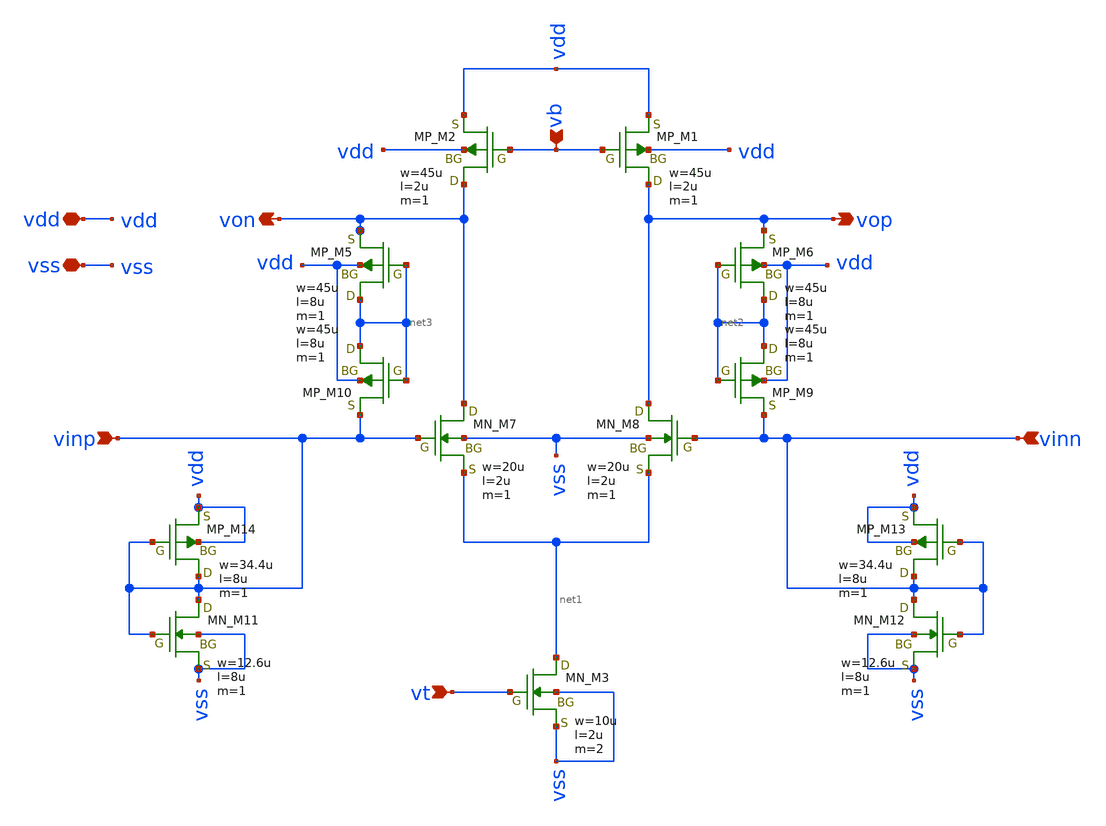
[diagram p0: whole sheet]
** sch_path: member_project/JJY_Receiver/Masahiro/jjy_recv/diff_amp/fully_diff_amp.sch
**.subckt fully_diff_amp vop von vinp vb vt vinn vdd vss
*.opin vop
*.opin von
*.ipin vinp
*.ipin vb
*.ipin vt
*.ipin vinn
*.iopin vdd
*.iopin vss
XM1 vop vb vdd vdd PMOS w=45u l=2u as=0 ad=0 ps=0 pd=0 nrd=0 nrs=0 m=1
XM2 von vb vdd vdd PMOS w=45u l=2u as=0 ad=0 ps=0 pd=0 nrd=0 nrs=0 m=1
XM3 net1 vt vss vss NMOS w=10u l=2u as=0 ad=0 ps=0 pd=0 nrd=0 nrs=0 m=2
XM7 von vinp net1 vss NMOS w=20u l=2u as=0 ad=0 ps=0 pd=0 nrd=0 nrs=0 m=1
XM8 vop vinn net1 vss NMOS w=20u l=2u as=0 ad=0 ps=0 pd=0 nrd=0 nrs=0 m=1
XM6 net2 net2 vop vdd PMOS w=45u l=8u as=0 ad=0 ps=0 pd=0 nrd=0 nrs=0 m=1
XM9 net2 net2 vinn vdd PMOS w=45u l=8u as=0 ad=0 ps=0 pd=0 nrd=0 nrs=0 m=1
XM5 net3 net3 von vdd PMOS w=45u l=8u as=0 ad=0 ps=0 pd=0 nrd=0 nrs=0 m=1
XM10 net3 net3 vinp vdd PMOS w=45u l=8u as=0 ad=0 ps=0 pd=0 nrd=0 nrs=0 m=1
XM12 vinn vinn vss vss NMOS w=12.6u l=8u as=0 ad=0 ps=0 pd=0 nrd=0 nrs=0 m=1
XM13 vinn vinn vdd vdd PMOS w=34.4u l=8u as=0 ad=0 ps=0 pd=0 nrd=0 nrs=0 m=1
XM11 vinp vinp vss vss NMOS w=12.6u l=8u as=0 ad=0 ps=0 pd=0 nrd=0 nrs=0 m=1
XM14 vinp vinp vdd vdd PMOS w=34.4u l=8u as=0 ad=0 ps=0 pd=0 nrd=0 nrs=0 m=1
**.ends
.end
